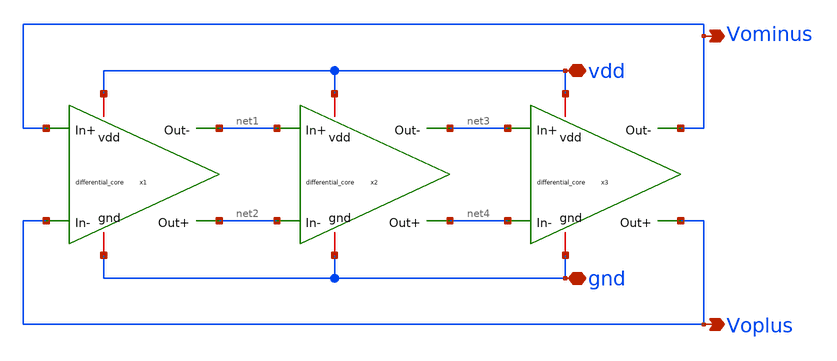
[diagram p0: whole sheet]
** sch_path: modules/module_4_type_2_PLL/diff_Roscillator/xschem/diff_ring_oscillator.sch
**.subckt diff_ring_oscillator Voplus Vominus vdd gnd
*.opin Voplus
*.opin Vominus
*.iopin vdd
*.iopin gnd
x1 vdd net2 net1 Vominus Voplus gnd differential_core
x2 vdd net4 net3 net1 net2 gnd differential_core
x3 vdd Voplus Vominus net3 net4 gnd differential_core
**.ends

* expanding   symbol:  differential_core.sym # of pins=6
** sym_path: modules/module_4_type_2_PLL/diff_Roscillator/schematic/differential_core.sym
** sch_path: modules/module_4_type_2_PLL/diff_Roscillator/schematic/differential_core.sch
.subckt differential_core vdd Out+ Out- In+ In- gnd
*.ipin In+
*.iopin vdd
*.iopin gnd
*.ipin In-
*.opin Out+
*.opin Out-
XM1 Out+ In- net1 gnd sg13_lv_nmos w=2.6u l=0.26u ng=1 m=1 mm_ok=1
XM2 Out- In+ net1 gnd sg13_lv_nmos w=2.6u l=0.26u ng=1 m=1 mm_ok=1
R1 vdd Out- 5k m=1
R2 vdd Out+ 5k m=1
C1 Out- gnd 0.5f m=1
C2 Out+ gnd 0.5f m=1
I0 net1 gnd 200u
.ends

.end
